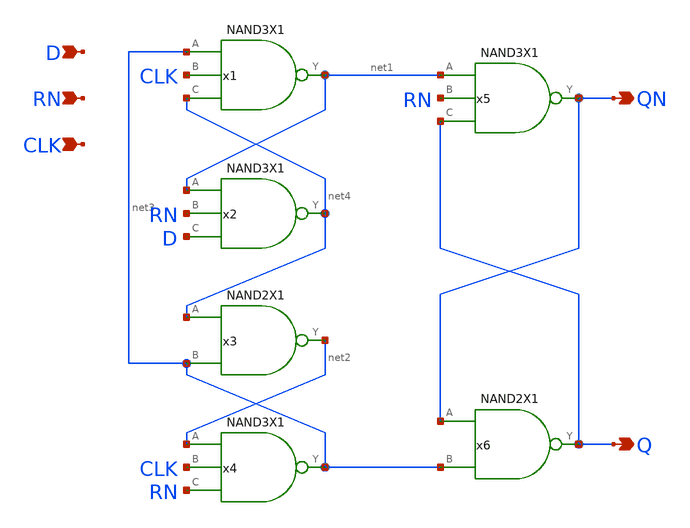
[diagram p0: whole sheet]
** sch_path: lib/xschem/DFFRNX1.sch
**.subckt DFFRNX1 D QN RN CLK Q
*.ipin D
*.opin QN
*.ipin RN
*.ipin CLK
*.opin Q
x2 net4 net1 RN D VDD VSS NAND3X1
x1 net1 net3 CLK net4 VDD VSS NAND3X1
x3 net2 net4 net3 VDD VSS NAND2X1
x4 net3 net2 CLK RN VDD VSS NAND3X1
x5 QN net1 RN Q VDD VSS NAND3X1
x6 Q QN net3 VDD VSS NAND2X1
**.ends

* expanding   symbol:  NAND3X1.sym # of pins=4
** sym_path: lib/xschem/NAND3X1.sym
** sch_path: lib/xschem/NAND3X1.sch
.subckt NAND3X1 Y A B C VDD VSS
*.ipin A
*.opin Y
*.ipin B
*.ipin C
XM1 net2 C VSS VSS sky130_fd_pr__nfet_01v8 L=0.15 W=3 nf=1 ad='int((nf+1)/2) * W/nf * 0.29' as='int((nf+2)/2) * W/nf * 0.29'
+ pd='2*int((nf+1)/2) * (W/nf + 0.29)' ps='2*int((nf+2)/2) * (W/nf + 0.29)' nrd='0.29 / W' nrs='0.29 / W'
+ sa=0 sb=0 sd=0 mult=1 m=1
XM2 Y A VDD VDD sky130_fd_pr__pfet_01v8 L=0.15 W=2 nf=1 ad='int((nf+1)/2) * W/nf * 0.29' as='int((nf+2)/2) * W/nf * 0.29'
+ pd='2*int((nf+1)/2) * (W/nf + 0.29)' ps='2*int((nf+2)/2) * (W/nf + 0.29)' nrd='0.29 / W' nrs='0.29 / W'
+ sa=0 sb=0 sd=0 mult=1 m=1
XM3 net1 B net2 VSS sky130_fd_pr__nfet_01v8 L=0.15 W=3 nf=1 ad='int((nf+1)/2) * W/nf * 0.29' as='int((nf+2)/2) * W/nf * 0.29'
+ pd='2*int((nf+1)/2) * (W/nf + 0.29)' ps='2*int((nf+2)/2) * (W/nf + 0.29)' nrd='0.29 / W' nrs='0.29 / W'
+ sa=0 sb=0 sd=0 mult=1 m=1
XM4 Y A net1 VSS sky130_fd_pr__nfet_01v8 L=0.15 W=3 nf=1 ad='int((nf+1)/2) * W/nf * 0.29' as='int((nf+2)/2) * W/nf * 0.29'
+ pd='2*int((nf+1)/2) * (W/nf + 0.29)' ps='2*int((nf+2)/2) * (W/nf + 0.29)' nrd='0.29 / W' nrs='0.29 / W'
+ sa=0 sb=0 sd=0 mult=1 m=1
XM5 Y A VDD VDD sky130_fd_pr__pfet_01v8 L=0.15 W=2 nf=1 ad='int((nf+1)/2) * W/nf * 0.29' as='int((nf+2)/2) * W/nf * 0.29'
+ pd='2*int((nf+1)/2) * (W/nf + 0.29)' ps='2*int((nf+2)/2) * (W/nf + 0.29)' nrd='0.29 / W' nrs='0.29 / W'
+ sa=0 sb=0 sd=0 mult=1 m=1
XM6 Y B VDD VDD sky130_fd_pr__pfet_01v8 L=0.15 W=2 nf=1 ad='int((nf+1)/2) * W/nf * 0.29' as='int((nf+2)/2) * W/nf * 0.29'
+ pd='2*int((nf+1)/2) * (W/nf + 0.29)' ps='2*int((nf+2)/2) * (W/nf + 0.29)' nrd='0.29 / W' nrs='0.29 / W'
+ sa=0 sb=0 sd=0 mult=1 m=1
XM7 Y B VDD VDD sky130_fd_pr__pfet_01v8 L=0.15 W=2 nf=1 ad='int((nf+1)/2) * W/nf * 0.29' as='int((nf+2)/2) * W/nf * 0.29'
+ pd='2*int((nf+1)/2) * (W/nf + 0.29)' ps='2*int((nf+2)/2) * (W/nf + 0.29)' nrd='0.29 / W' nrs='0.29 / W'
+ sa=0 sb=0 sd=0 mult=1 m=1
XM8 Y C VDD VDD sky130_fd_pr__pfet_01v8 L=0.15 W=2 nf=1 ad='int((nf+1)/2) * W/nf * 0.29' as='int((nf+2)/2) * W/nf * 0.29'
+ pd='2*int((nf+1)/2) * (W/nf + 0.29)' ps='2*int((nf+2)/2) * (W/nf + 0.29)' nrd='0.29 / W' nrs='0.29 / W'
+ sa=0 sb=0 sd=0 mult=1 m=1
XM9 Y C VDD VDD sky130_fd_pr__pfet_01v8 L=0.15 W=2 nf=1 ad='int((nf+1)/2) * W/nf * 0.29' as='int((nf+2)/2) * W/nf * 0.29'
+ pd='2*int((nf+1)/2) * (W/nf + 0.29)' ps='2*int((nf+2)/2) * (W/nf + 0.29)' nrd='0.29 / W' nrs='0.29 / W'
+ sa=0 sb=0 sd=0 mult=1 m=1
.ends


* expanding   symbol:  NAND2X1.sym # of pins=3
** sym_path: lib/xschem/NAND2X1.sym
** sch_path: lib/xschem/NAND2X1.sch
.subckt NAND2X1 Y A B VDD VSS
*.ipin A
*.opin Y
*.ipin B
XM1 Y A VDD VDD sky130_fd_pr__pfet_01v8 L=0.15 W=2 nf=1 ad='int((nf+1)/2) * W/nf * 0.29' as='int((nf+2)/2) * W/nf * 0.29'
+ pd='2*int((nf+1)/2) * (W/nf + 0.29)' ps='2*int((nf+2)/2) * (W/nf + 0.29)' nrd='0.29 / W' nrs='0.29 / W'
+ sa=0 sb=0 sd=0 mult=1 m=1
XM5 Y A net1 VSS sky130_fd_pr__nfet_01v8 L=0.15 W=3 nf=1 ad='int((nf+1)/2) * W/nf * 0.29' as='int((nf+2)/2) * W/nf * 0.29'
+ pd='2*int((nf+1)/2) * (W/nf + 0.29)' ps='2*int((nf+2)/2) * (W/nf + 0.29)' nrd='0.29 / W' nrs='0.29 / W'
+ sa=0 sb=0 sd=0 mult=1 m=1
XM2 Y A VDD VDD sky130_fd_pr__pfet_01v8 L=0.15 W=2 nf=1 ad='int((nf+1)/2) * W/nf * 0.29' as='int((nf+2)/2) * W/nf * 0.29'
+ pd='2*int((nf+1)/2) * (W/nf + 0.29)' ps='2*int((nf+2)/2) * (W/nf + 0.29)' nrd='0.29 / W' nrs='0.29 / W'
+ sa=0 sb=0 sd=0 mult=1 m=1
XM3 Y B VDD VDD sky130_fd_pr__pfet_01v8 L=0.15 W=2 nf=1 ad='int((nf+1)/2) * W/nf * 0.29' as='int((nf+2)/2) * W/nf * 0.29'
+ pd='2*int((nf+1)/2) * (W/nf + 0.29)' ps='2*int((nf+2)/2) * (W/nf + 0.29)' nrd='0.29 / W' nrs='0.29 / W'
+ sa=0 sb=0 sd=0 mult=1 m=1
XM4 Y B VDD VDD sky130_fd_pr__pfet_01v8 L=0.15 W=2 nf=1 ad='int((nf+1)/2) * W/nf * 0.29' as='int((nf+2)/2) * W/nf * 0.29'
+ pd='2*int((nf+1)/2) * (W/nf + 0.29)' ps='2*int((nf+2)/2) * (W/nf + 0.29)' nrd='0.29 / W' nrs='0.29 / W'
+ sa=0 sb=0 sd=0 mult=1 m=1
XM6 net1 B VSS VSS sky130_fd_pr__nfet_01v8 L=0.15 W=3 nf=1 ad='int((nf+1)/2) * W/nf * 0.29' as='int((nf+2)/2) * W/nf * 0.29'
+ pd='2*int((nf+1)/2) * (W/nf + 0.29)' ps='2*int((nf+2)/2) * (W/nf + 0.29)' nrd='0.29 / W' nrs='0.29 / W'
+ sa=0 sb=0 sd=0 mult=1 m=1
.ends

.end
